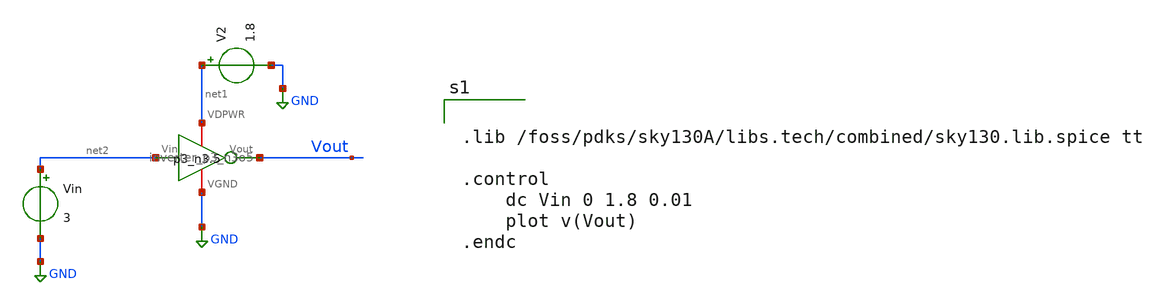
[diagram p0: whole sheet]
** sch_path: xschem/unit_inverter_test.sch
**.subckt unit_inverter_test
Vin net2 GND 3
V2 net1 GND 1.8
x1 net1 Vout net2 GND inverter_p3_n3o5
**** begin user architecture code


.lib /foss/pdks/sky130A/libs.tech/combined/sky130.lib.spice tt

.control
	dc Vin 0 1.8 0.01
	plot v(Vout)
.endc


**** end user architecture code
**.ends

* expanding   symbol:
*+  /foss/designs/analog-circuit-design/sky25a-TIQ_ADC/xschem/INVERTER_SIZES/inverter_p3_n3o5.sym # of pins=4
** sym_path: xschem/INVERTER_SIZES/inverter_p3_n3o5.sym
** sch_path: xschem/INVERTER_SIZES/inverter_p3_n3o5.sch
.subckt inverter_p3_n3o5 VDPWR Vout Vin VGND
*.opin Vout
*.ipin Vin
*.iopin VDPWR
*.iopin VGND
XM1 Vout Vin VGND VGND sky130_fd_pr__nfet_01v8 L=0.15 W=3.5 nf=1 ad='int((nf+1)/2) * W/nf * 0.29' as='int((nf+2)/2) * W/nf * 0.29'
+ pd='2*int((nf+1)/2) * (W/nf + 0.29)' ps='2*int((nf+2)/2) * (W/nf + 0.29)' nrd='0.29 / W' nrs='0.29 / W'
+ sa=0 sb=0 sd=0 mult=1 m=1
XM2 Vout Vin VDPWR VDPWR sky130_fd_pr__pfet_01v8 L=0.15 W=3 nf=1 ad='int((nf+1)/2) * W/nf * 0.29' as='int((nf+2)/2) * W/nf * 0.29'
+ pd='2*int((nf+1)/2) * (W/nf + 0.29)' ps='2*int((nf+2)/2) * (W/nf + 0.29)' nrd='0.29 / W' nrs='0.29 / W'
+ sa=0 sb=0 sd=0 mult=1 m=1
.ends

.GLOBAL GND
.end
